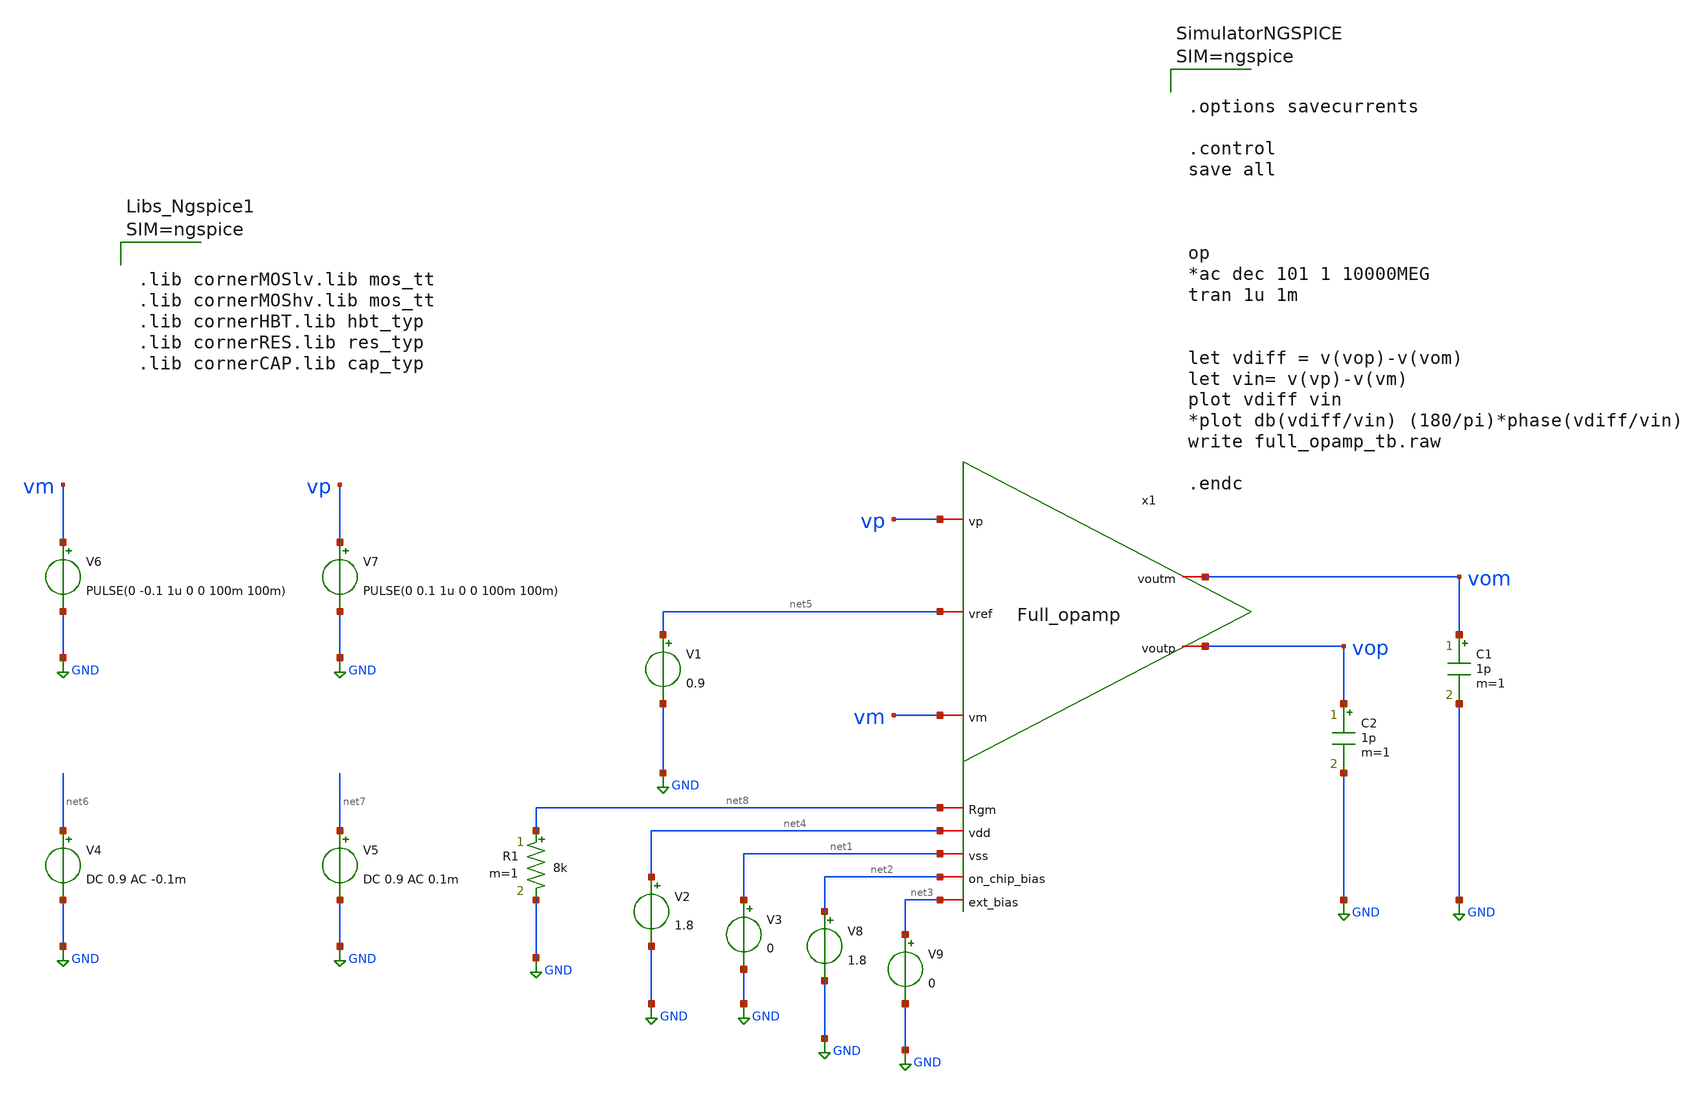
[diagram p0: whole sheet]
** sch_path: LVS/Unic_cass_final_design_lvs/Simulations/Opamp_design/testbench/full_opamp_tb.sch
**.subckt full_opamp_tb
x1 net2 net5 net4 vom net3 vm vop net1 vp net8 Full_opamp
V4 net6 GND DC 0.9 AC -0.1m
V5 net7 GND DC 0.9 AC 0.1m
V6 vm GND PULSE(0 -0.1 1u 0 0 100m 100m)
V7 vp GND PULSE(0 0.1 1u 0 0 100m 100m)
C1 vom GND 1p m=1
C2 vop GND 1p m=1
V1 net5 GND 0.9
V2 net4 GND 1.8
V3 net1 GND 0
V8 net2 GND 1.8
V9 net3 GND 0
R1 net8 GND 8k m=1
**** begin user architecture code



.lib cornerMOSlv.lib mos_tt
.lib cornerMOShv.lib mos_tt
.lib cornerHBT.lib hbt_typ
.lib cornerRES.lib res_typ
.lib cornerCAP.lib cap_typ



**** end user architecture code
**.ends
.GLOBAL GND
**** begin user architecture code



.options savecurrents

.control
save all



op
*ac dec 101 1 10000MEG
tran 1u 1m


let vdiff = v(vop)-v(vom)
let vin= v(vp)-v(vm)
plot vdiff vin
*plot db(vdiff/vin) (180/pi)*phase(vdiff/vin)
write full_opamp_tb.raw

.endc



**** end user architecture code
.end
